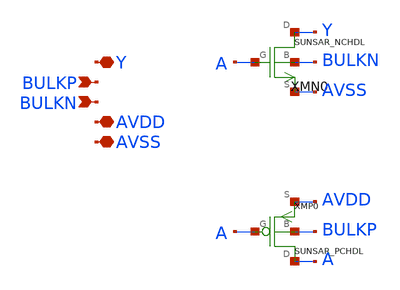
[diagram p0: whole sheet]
** sch_path: ip/sun_sar9b_sky130nm/design/SUN_SAR9B_SKY130NM/SUNSAR_TIEL_CV.sch
**.subckt SUNSAR_TIEL_CV Y BULKP BULKN AVDD AVSS
*.iopin Y
*.ipin BULKP
*.ipin BULKN
*.iopin AVDD
*.iopin AVSS
XMN0 Y A AVSS BULKN SUNSAR_NCHDL
XMP0 A A AVDD BULKP SUNSAR_PCHDL
**.ends
.end
